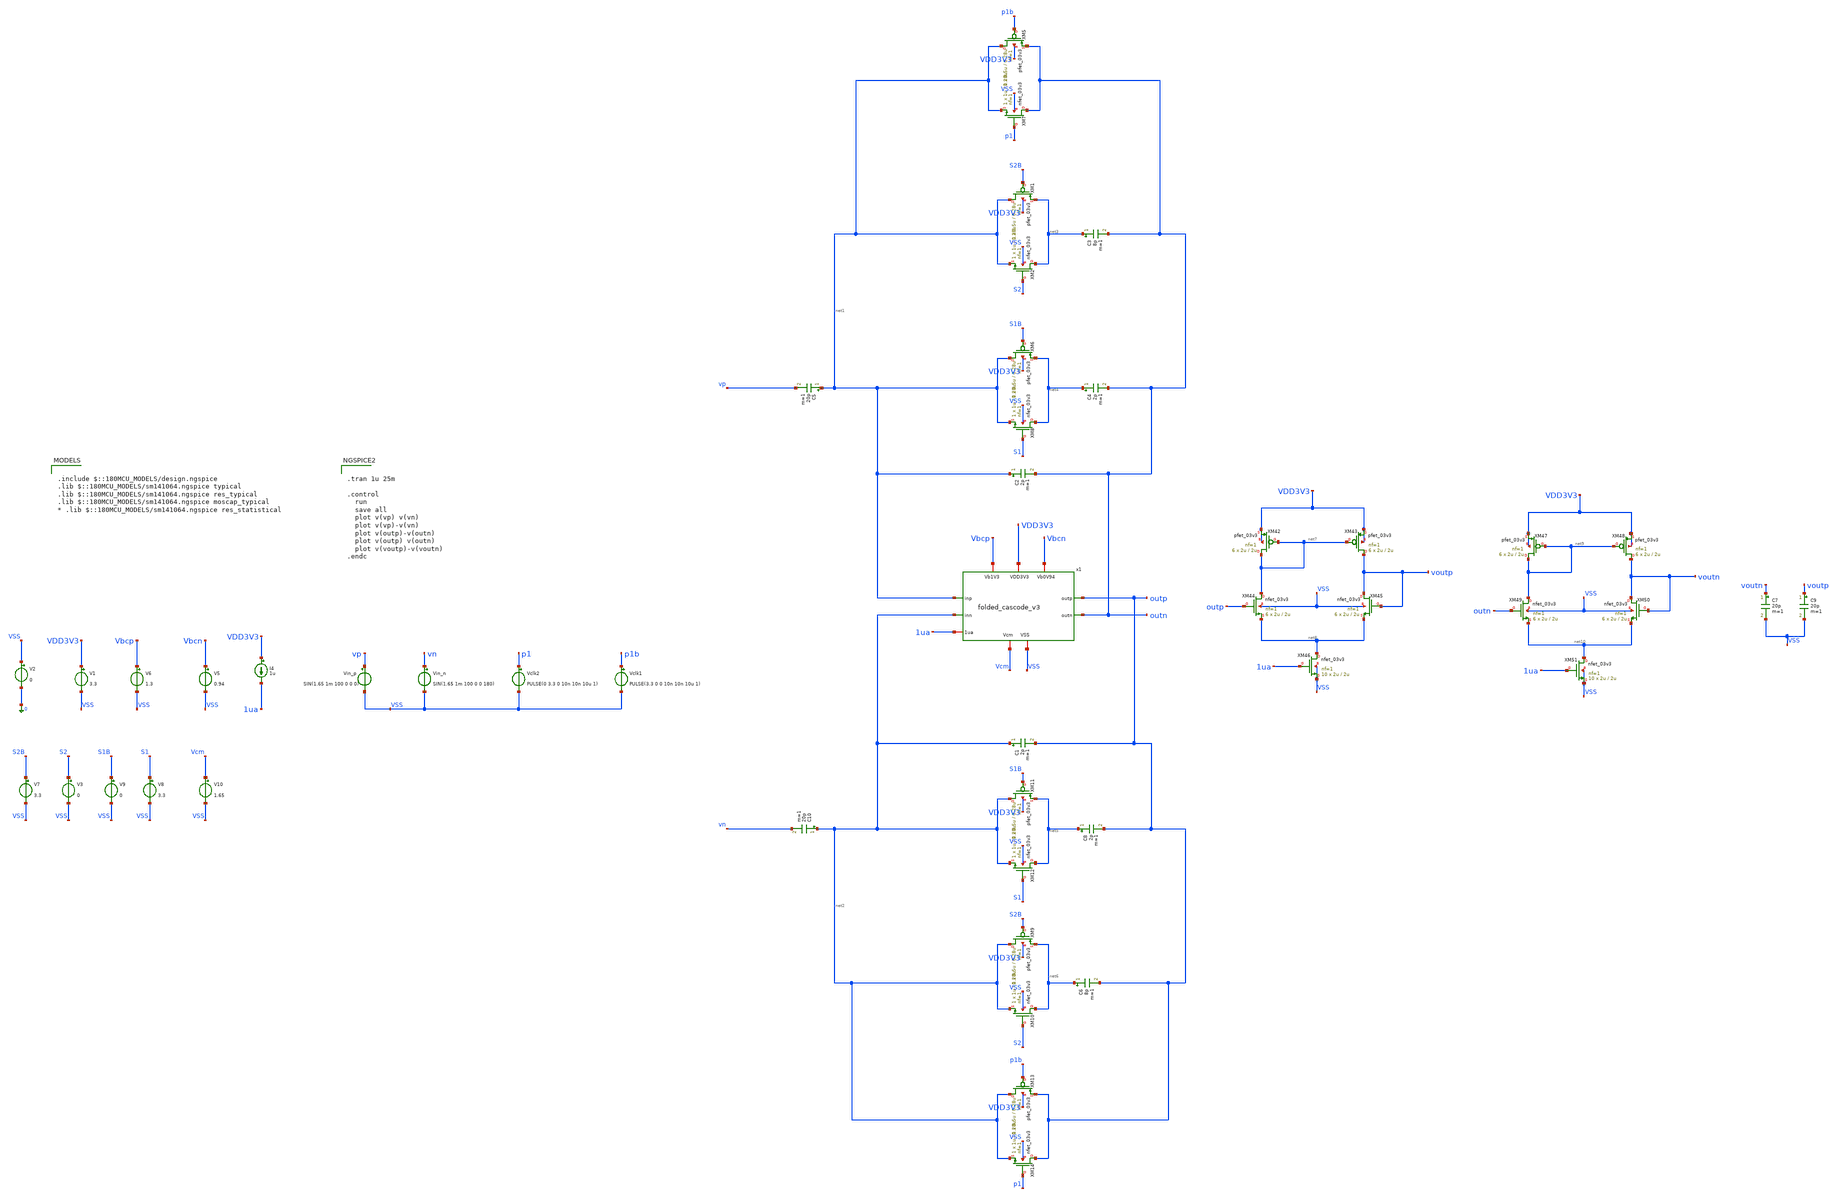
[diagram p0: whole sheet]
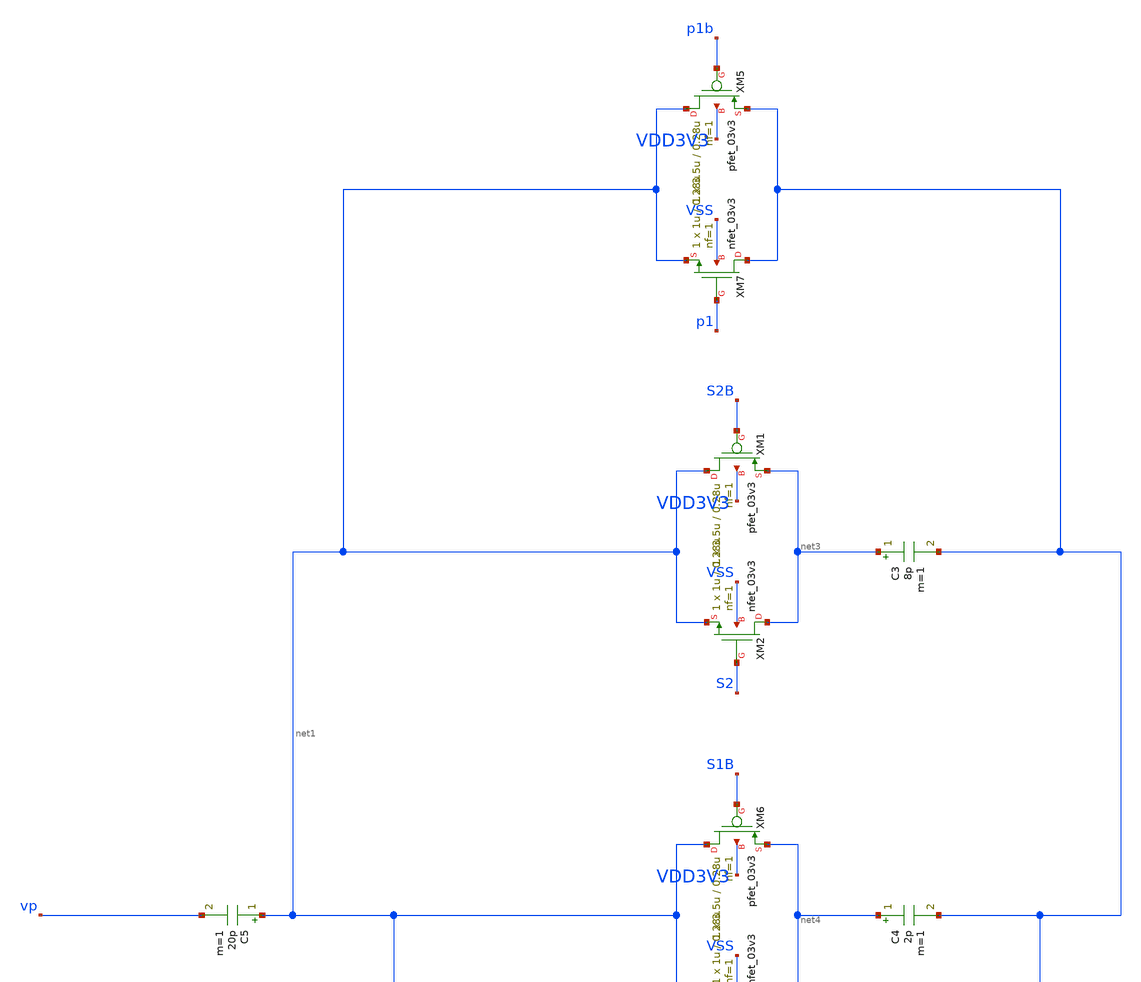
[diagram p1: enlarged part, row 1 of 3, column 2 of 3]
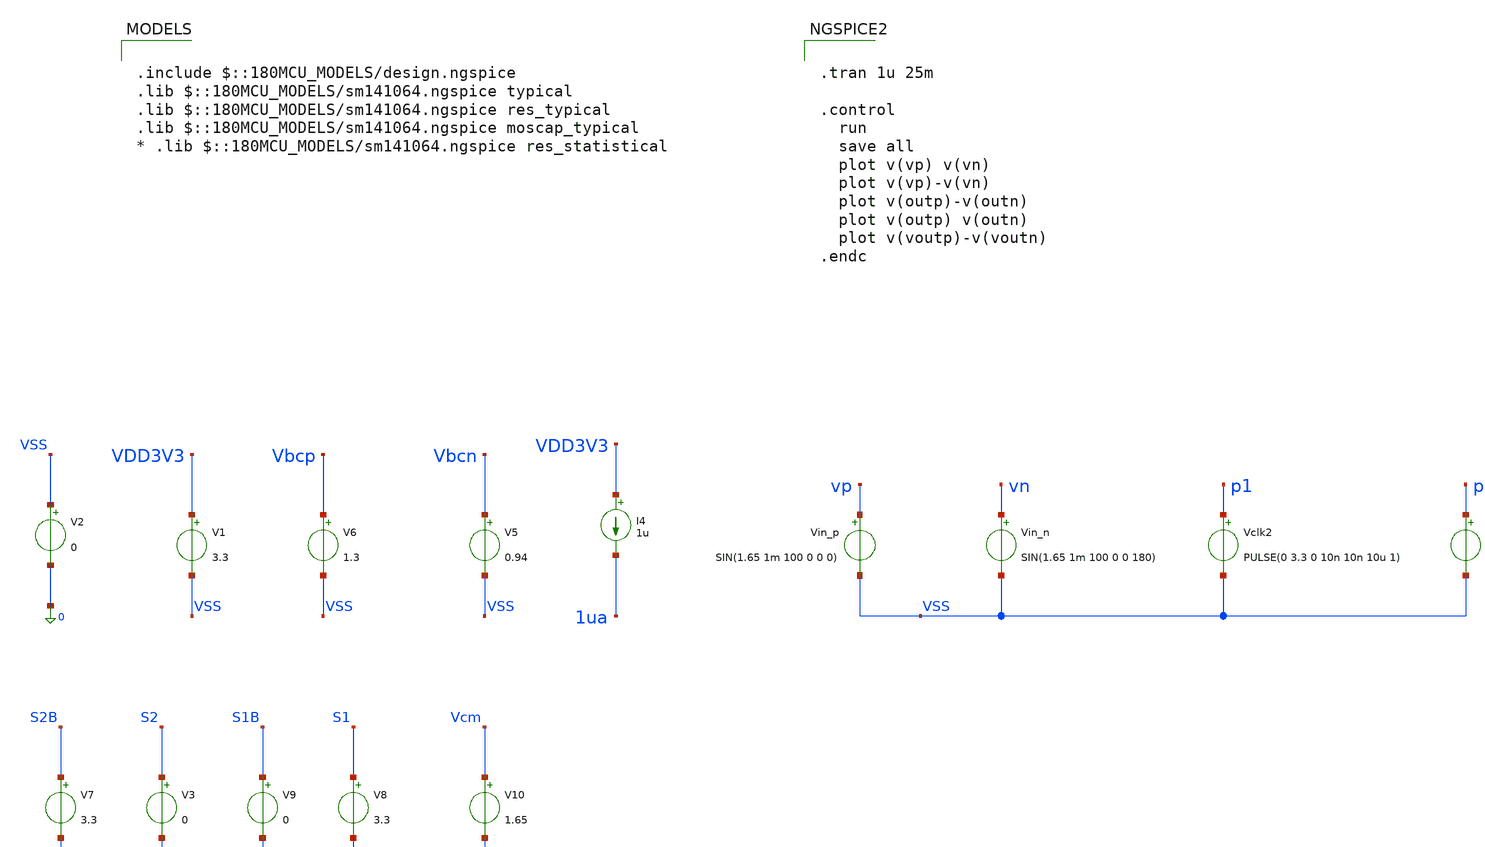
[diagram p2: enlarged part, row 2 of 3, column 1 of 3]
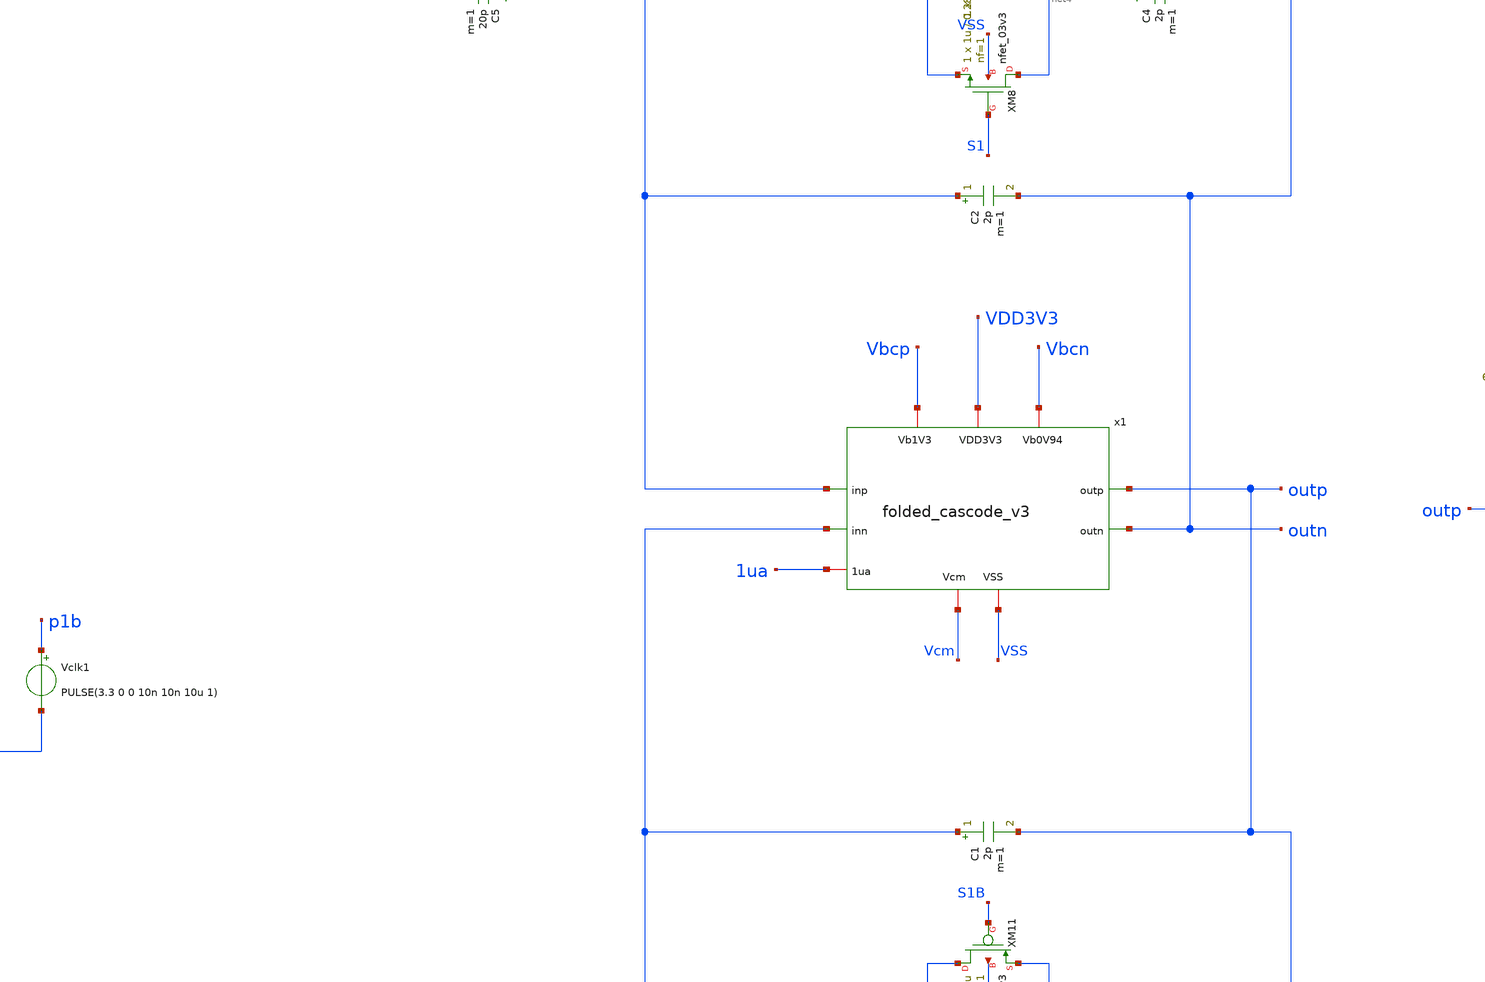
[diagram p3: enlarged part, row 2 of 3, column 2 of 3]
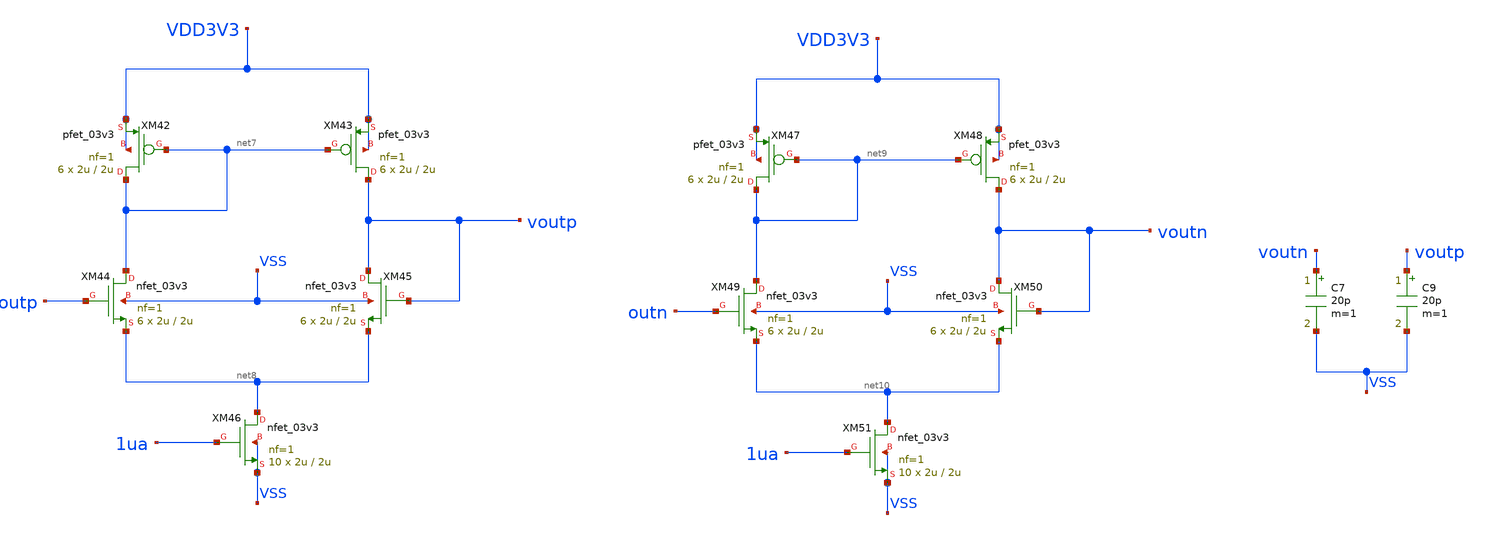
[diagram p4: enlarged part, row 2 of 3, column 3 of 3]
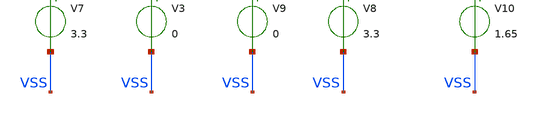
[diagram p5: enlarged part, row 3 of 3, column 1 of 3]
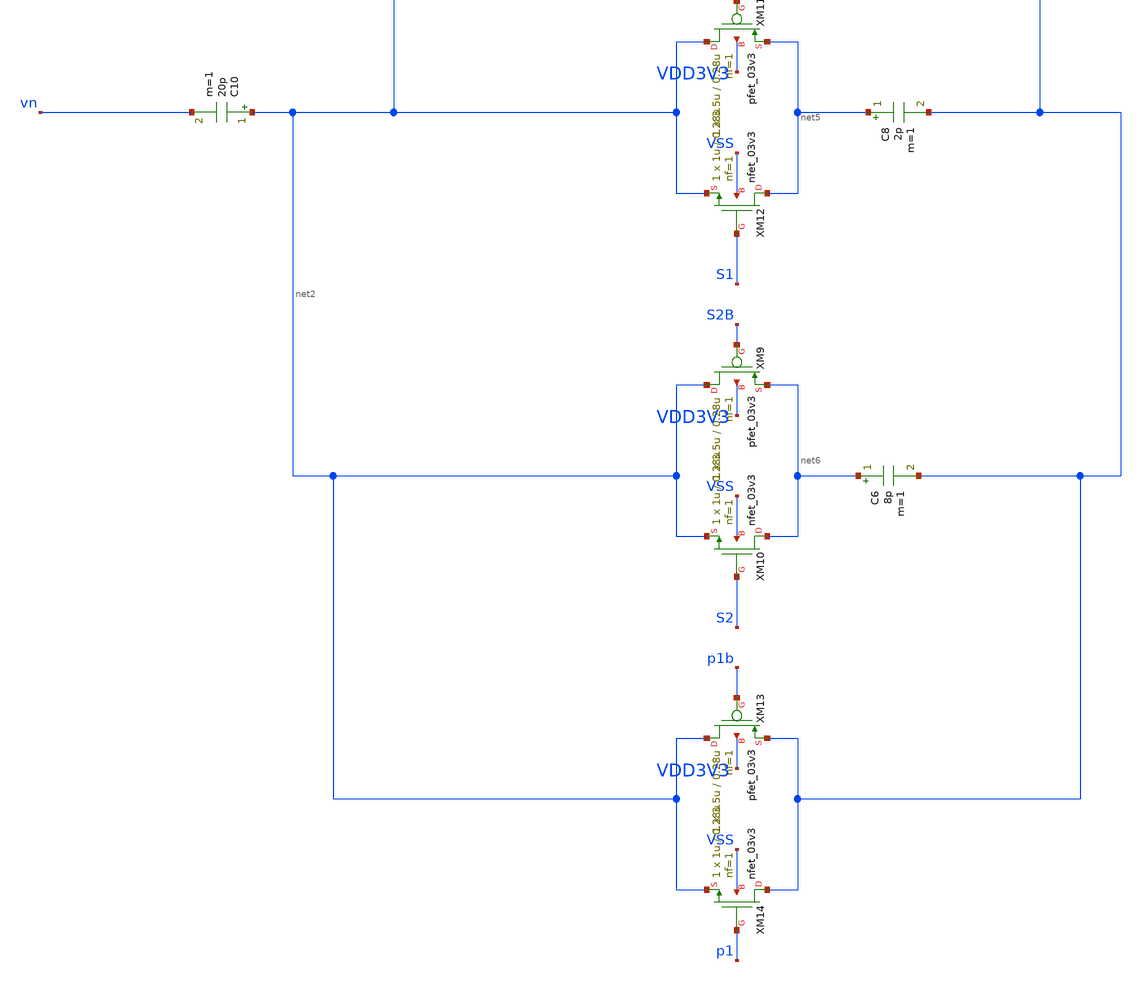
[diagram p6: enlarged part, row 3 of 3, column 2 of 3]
** sch_path: designs/libs/tb_pga/tb_pga_v3.sch
**.subckt tb_pga_v3
I4 VDD3V3 1ua 1u
V5 Vbcn VSS 0.94
V6 Vbcp VSS 1.3
V1 VDD3V3 VSS 3.3
V2 VSS 0 0
C3 net3 outn 8p m=1
C5 net1 vp 20p m=1
C10 net2 vn 20p m=1
C4 net4 outn 2p m=1
XM1 net1 S2B net3 VDD3V3 pfet_03v3 L=0.28u W=3.5u nf=1 ad='int((nf+1)/2) * W/nf * 0.18u' as='int((nf+2)/2) * W/nf * 0.18u'
+ pd='2*int((nf+1)/2) * (W/nf + 0.18u)' ps='2*int((nf+2)/2) * (W/nf + 0.18u)' nrd='0.18u / W' nrs='0.18u / W'
+ sa=0 sb=0 sd=0 m=1
XM2 net3 S2 net1 VSS nfet_03v3 L=0.28u W=1u nf=1 ad='int((nf+1)/2) * W/nf * 0.18u' as='int((nf+2)/2) * W/nf * 0.18u'
+ pd='2*int((nf+1)/2) * (W/nf + 0.18u)' ps='2*int((nf+2)/2) * (W/nf + 0.18u)' nrd='0.18u / W' nrs='0.18u / W'
+ sa=0 sb=0 sd=0 m=1
C1 net2 outp 2p m=1
C6 net6 outp 8p m=1
XM6 net1 S1B net4 VDD3V3 pfet_03v3 L=0.28u W=3.5u nf=1 ad='int((nf+1)/2) * W/nf * 0.18u' as='int((nf+2)/2) * W/nf * 0.18u'
+ pd='2*int((nf+1)/2) * (W/nf + 0.18u)' ps='2*int((nf+2)/2) * (W/nf + 0.18u)' nrd='0.18u / W' nrs='0.18u / W'
+ sa=0 sb=0 sd=0 m=1
XM8 net4 S1 net1 VSS nfet_03v3 L=0.28u W=1u nf=1 ad='int((nf+1)/2) * W/nf * 0.18u' as='int((nf+2)/2) * W/nf * 0.18u'
+ pd='2*int((nf+1)/2) * (W/nf + 0.18u)' ps='2*int((nf+2)/2) * (W/nf + 0.18u)' nrd='0.18u / W' nrs='0.18u / W'
+ sa=0 sb=0 sd=0 m=1
XM9 net2 S2B net6 VDD3V3 pfet_03v3 L=0.28u W=3.5u nf=1 ad='int((nf+1)/2) * W/nf * 0.18u' as='int((nf+2)/2) * W/nf * 0.18u'
+ pd='2*int((nf+1)/2) * (W/nf + 0.18u)' ps='2*int((nf+2)/2) * (W/nf + 0.18u)' nrd='0.18u / W' nrs='0.18u / W'
+ sa=0 sb=0 sd=0 m=1
XM10 net6 S2 net2 VSS nfet_03v3 L=0.28u W=1u nf=1 ad='int((nf+1)/2) * W/nf * 0.18u' as='int((nf+2)/2) * W/nf * 0.18u'
+ pd='2*int((nf+1)/2) * (W/nf + 0.18u)' ps='2*int((nf+2)/2) * (W/nf + 0.18u)' nrd='0.18u / W' nrs='0.18u / W'
+ sa=0 sb=0 sd=0 m=1
XM11 net2 S1B net5 VDD3V3 pfet_03v3 L=0.28u W=3.5u nf=1 ad='int((nf+1)/2) * W/nf * 0.18u' as='int((nf+2)/2) * W/nf * 0.18u'
+ pd='2*int((nf+1)/2) * (W/nf + 0.18u)' ps='2*int((nf+2)/2) * (W/nf + 0.18u)' nrd='0.18u / W' nrs='0.18u / W'
+ sa=0 sb=0 sd=0 m=1
XM12 net5 S1 net2 VSS nfet_03v3 L=0.28u W=1u nf=1 ad='int((nf+1)/2) * W/nf * 0.18u' as='int((nf+2)/2) * W/nf * 0.18u'
+ pd='2*int((nf+1)/2) * (W/nf + 0.18u)' ps='2*int((nf+2)/2) * (W/nf + 0.18u)' nrd='0.18u / W' nrs='0.18u / W'
+ sa=0 sb=0 sd=0 m=1
Vin_p vp VSS SIN(1.65 1m 100 0 0 0)
Vin_n vn VSS SIN(1.65 1m 100 0 0 180)
V7 S2B VSS 3.3
V8 S1 VSS 3.3
V9 S1B VSS 0
V10 Vcm VSS 1.65
C7 voutn VSS 20p m=1
C9 voutp VSS 20p m=1
V3 S2 VSS 0
C8 net5 outp 2p m=1
C2 net1 outn 2p m=1
XM5 net1 p1b outn VDD3V3 pfet_03v3 L=0.28u W=3.5u nf=1 ad='int((nf+1)/2) * W/nf * 0.18u' as='int((nf+2)/2) * W/nf * 0.18u'
+ pd='2*int((nf+1)/2) * (W/nf + 0.18u)' ps='2*int((nf+2)/2) * (W/nf + 0.18u)' nrd='0.18u / W' nrs='0.18u / W'
+ sa=0 sb=0 sd=0 m=1
XM7 outn p1 net1 VSS nfet_03v3 L=0.28u W=1u nf=1 ad='int((nf+1)/2) * W/nf * 0.18u' as='int((nf+2)/2) * W/nf * 0.18u'
+ pd='2*int((nf+1)/2) * (W/nf + 0.18u)' ps='2*int((nf+2)/2) * (W/nf + 0.18u)' nrd='0.18u / W' nrs='0.18u / W'
+ sa=0 sb=0 sd=0 m=1
XM13 net2 p1b outp VDD3V3 pfet_03v3 L=0.28u W=3.5u nf=1 ad='int((nf+1)/2) * W/nf * 0.18u' as='int((nf+2)/2) * W/nf * 0.18u'
+ pd='2*int((nf+1)/2) * (W/nf + 0.18u)' ps='2*int((nf+2)/2) * (W/nf + 0.18u)' nrd='0.18u / W' nrs='0.18u / W'
+ sa=0 sb=0 sd=0 m=1
XM14 outp p1 net2 VSS nfet_03v3 L=0.28u W=1u nf=1 ad='int((nf+1)/2) * W/nf * 0.18u' as='int((nf+2)/2) * W/nf * 0.18u'
+ pd='2*int((nf+1)/2) * (W/nf + 0.18u)' ps='2*int((nf+2)/2) * (W/nf + 0.18u)' nrd='0.18u / W' nrs='0.18u / W'
+ sa=0 sb=0 sd=0 m=1
Vclk2 p1 VSS PULSE(0 3.3 0 10n 10n 10u 1)
Vclk1 p1b VSS PULSE(3.3 0 0 10n 10n 10u 1)
XM42 net7 net7 VDD3V3 VDD3V3 pfet_03v3 L=2u W=2u nf=1 ad='int((nf+1)/2) * W/nf * 0.18u' as='int((nf+2)/2) * W/nf * 0.18u'
+ pd='2*int((nf+1)/2) * (W/nf + 0.18u)' ps='2*int((nf+2)/2) * (W/nf + 0.18u)' nrd='0.18u / W' nrs='0.18u / W'
+ sa=0 sb=0 sd=0 m=6
XM43 voutp net7 VDD3V3 VDD3V3 pfet_03v3 L=2u W=2u nf=1 ad='int((nf+1)/2) * W/nf * 0.18u' as='int((nf+2)/2) * W/nf * 0.18u'
+ pd='2*int((nf+1)/2) * (W/nf + 0.18u)' ps='2*int((nf+2)/2) * (W/nf + 0.18u)' nrd='0.18u / W' nrs='0.18u / W'
+ sa=0 sb=0 sd=0 m=6
XM44 net7 outp net8 VSS nfet_03v3 L=2u W=2u nf=1 ad='int((nf+1)/2) * W/nf * 0.18u' as='int((nf+2)/2) * W/nf * 0.18u'
+ pd='2*int((nf+1)/2) * (W/nf + 0.18u)' ps='2*int((nf+2)/2) * (W/nf + 0.18u)' nrd='0.18u / W' nrs='0.18u / W'
+ sa=0 sb=0 sd=0 m=6
XM45 voutp voutp net8 VSS nfet_03v3 L=2u W=2u nf=1 ad='int((nf+1)/2) * W/nf * 0.18u' as='int((nf+2)/2) * W/nf * 0.18u'
+ pd='2*int((nf+1)/2) * (W/nf + 0.18u)' ps='2*int((nf+2)/2) * (W/nf + 0.18u)' nrd='0.18u / W' nrs='0.18u / W'
+ sa=0 sb=0 sd=0 m=6
XM46 net8 1ua VSS VSS nfet_03v3 L=2u W=2u nf=1 ad='int((nf+1)/2) * W/nf * 0.18u' as='int((nf+2)/2) * W/nf * 0.18u'
+ pd='2*int((nf+1)/2) * (W/nf + 0.18u)' ps='2*int((nf+2)/2) * (W/nf + 0.18u)' nrd='0.18u / W' nrs='0.18u / W'
+ sa=0 sb=0 sd=0 m=10
XM47 net9 net9 VDD3V3 VDD3V3 pfet_03v3 L=2u W=2u nf=1 ad='int((nf+1)/2) * W/nf * 0.18u' as='int((nf+2)/2) * W/nf * 0.18u'
+ pd='2*int((nf+1)/2) * (W/nf + 0.18u)' ps='2*int((nf+2)/2) * (W/nf + 0.18u)' nrd='0.18u / W' nrs='0.18u / W'
+ sa=0 sb=0 sd=0 m=6
XM48 voutn net9 VDD3V3 VDD3V3 pfet_03v3 L=2u W=2u nf=1 ad='int((nf+1)/2) * W/nf * 0.18u' as='int((nf+2)/2) * W/nf * 0.18u'
+ pd='2*int((nf+1)/2) * (W/nf + 0.18u)' ps='2*int((nf+2)/2) * (W/nf + 0.18u)' nrd='0.18u / W' nrs='0.18u / W'
+ sa=0 sb=0 sd=0 m=6
XM49 net9 outn net10 VSS nfet_03v3 L=2u W=2u nf=1 ad='int((nf+1)/2) * W/nf * 0.18u' as='int((nf+2)/2) * W/nf * 0.18u'
+ pd='2*int((nf+1)/2) * (W/nf + 0.18u)' ps='2*int((nf+2)/2) * (W/nf + 0.18u)' nrd='0.18u / W' nrs='0.18u / W'
+ sa=0 sb=0 sd=0 m=6
XM50 voutn voutn net10 VSS nfet_03v3 L=2u W=2u nf=1 ad='int((nf+1)/2) * W/nf * 0.18u' as='int((nf+2)/2) * W/nf * 0.18u'
+ pd='2*int((nf+1)/2) * (W/nf + 0.18u)' ps='2*int((nf+2)/2) * (W/nf + 0.18u)' nrd='0.18u / W' nrs='0.18u / W'
+ sa=0 sb=0 sd=0 m=6
XM51 net10 1ua VSS VSS nfet_03v3 L=2u W=2u nf=1 ad='int((nf+1)/2) * W/nf * 0.18u' as='int((nf+2)/2) * W/nf * 0.18u'
+ pd='2*int((nf+1)/2) * (W/nf + 0.18u)' ps='2*int((nf+2)/2) * (W/nf + 0.18u)' nrd='0.18u / W' nrs='0.18u / W'
+ sa=0 sb=0 sd=0 m=10
x1 outp outn VSS VDD3V3 net1 net2 1ua Vbcp Vbcn Vcm folded_cascode_v3
**** begin user architecture code


.tran 1u 25m

.control
  run
  save all
  plot v(vp) v(vn)
  plot v(vp)-v(vn)
  plot v(outp)-v(outn)
  plot v(outp) v(outn)
  plot v(voutp)-v(voutn)
.endc



.include $::180MCU_MODELS/design.ngspice
.lib $::180MCU_MODELS/sm141064.ngspice typical
.lib $::180MCU_MODELS/sm141064.ngspice res_typical
.lib $::180MCU_MODELS/sm141064.ngspice moscap_typical
* .lib $::180MCU_MODELS/sm141064.ngspice res_statistical

**** end user architecture code
**.ends
.end
